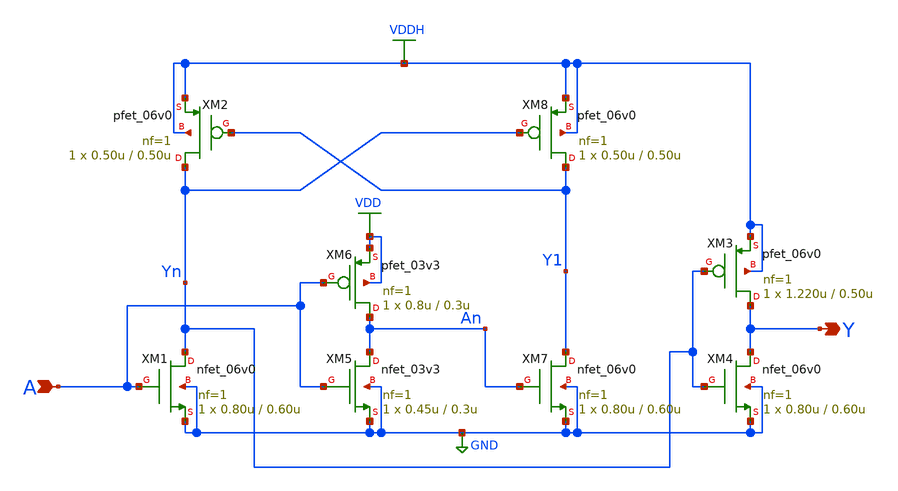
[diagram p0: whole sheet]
** sch_path: designs/libs/core_digital/gf180mcu_osu_sc_gp9t3v3/cells/lshifup/gf180mcu_osu_sc_gp9t3v3_lshifup.sch
**.subckt gf180mcu_osu_sc_gp9t3v3_lshifup A Y
*.ipin A
*.opin Y
XM1 Yn A GND GND nfet_06v0 L=0.60u W=0.80u nf=1 ad='int((nf+1)/2) * W/nf * 0.18u' as='int((nf+2)/2) * W/nf * 0.18u'
+ pd='2*int((nf+1)/2) * (W/nf + 0.18u)' ps='2*int((nf+2)/2) * (W/nf + 0.18u)' nrd='0.18u / W' nrs='0.18u / W'
+ sa=0 sb=0 sd=0 m=1
XM2 Yn Y1 VDDH VDDH pfet_06v0 L=0.50u W=0.50u nf=1 ad='int((nf+1)/2) * W/nf * 0.18u' as='int((nf+2)/2) * W/nf * 0.18u'
+ pd='2*int((nf+1)/2) * (W/nf + 0.18u)' ps='2*int((nf+2)/2) * (W/nf + 0.18u)' nrd='0.18u / W' nrs='0.18u / W'
+ sa=0 sb=0 sd=0 m=1
XM3 Y Yn VDDH VDDH pfet_06v0 L=0.50u W=1.220u nf=1 ad='int((nf+1)/2) * W/nf * 0.18u' as='int((nf+2)/2) * W/nf * 0.18u'
+ pd='2*int((nf+1)/2) * (W/nf + 0.18u)' ps='2*int((nf+2)/2) * (W/nf + 0.18u)' nrd='0.18u / W' nrs='0.18u / W'
+ sa=0 sb=0 sd=0 m=1
XM4 Y Yn GND GND nfet_06v0 L=0.60u W=0.80u nf=1 ad='int((nf+1)/2) * W/nf * 0.18u' as='int((nf+2)/2) * W/nf * 0.18u'
+ pd='2*int((nf+1)/2) * (W/nf + 0.18u)' ps='2*int((nf+2)/2) * (W/nf + 0.18u)' nrd='0.18u / W' nrs='0.18u / W'
+ sa=0 sb=0 sd=0 m=1
XM5 An A GND GND nfet_03v3 L=0.3u W=0.45u nf=1 ad='int((nf+1)/2) * W/nf * 0.18u' as='int((nf+2)/2) * W/nf * 0.18u'
+ pd='2*int((nf+1)/2) * (W/nf + 0.18u)' ps='2*int((nf+2)/2) * (W/nf + 0.18u)' nrd='0.18u / W' nrs='0.18u / W'
+ sa=0 sb=0 sd=0 m=1
XM6 An A VDD VDD pfet_03v3 L=0.3u W=0.8u nf=1 ad='int((nf+1)/2) * W/nf * 0.18u' as='int((nf+2)/2) * W/nf * 0.18u'
+ pd='2*int((nf+1)/2) * (W/nf + 0.18u)' ps='2*int((nf+2)/2) * (W/nf + 0.18u)' nrd='0.18u / W' nrs='0.18u / W'
+ sa=0 sb=0 sd=0 m=1
XM7 Y1 An GND GND nfet_06v0 L=0.60u W=0.80u nf=1 ad='int((nf+1)/2) * W/nf * 0.18u' as='int((nf+2)/2) * W/nf * 0.18u'
+ pd='2*int((nf+1)/2) * (W/nf + 0.18u)' ps='2*int((nf+2)/2) * (W/nf + 0.18u)' nrd='0.18u / W' nrs='0.18u / W'
+ sa=0 sb=0 sd=0 m=1
XM8 Y1 Yn VDDH VDDH pfet_06v0 L=0.50u W=0.50u nf=1 ad='int((nf+1)/2) * W/nf * 0.18u' as='int((nf+2)/2) * W/nf * 0.18u'
+ pd='2*int((nf+1)/2) * (W/nf + 0.18u)' ps='2*int((nf+2)/2) * (W/nf + 0.18u)' nrd='0.18u / W' nrs='0.18u / W'
+ sa=0 sb=0 sd=0 m=1
**.ends
.GLOBAL VDD
.GLOBAL GND
.GLOBAL VDDH
.end
